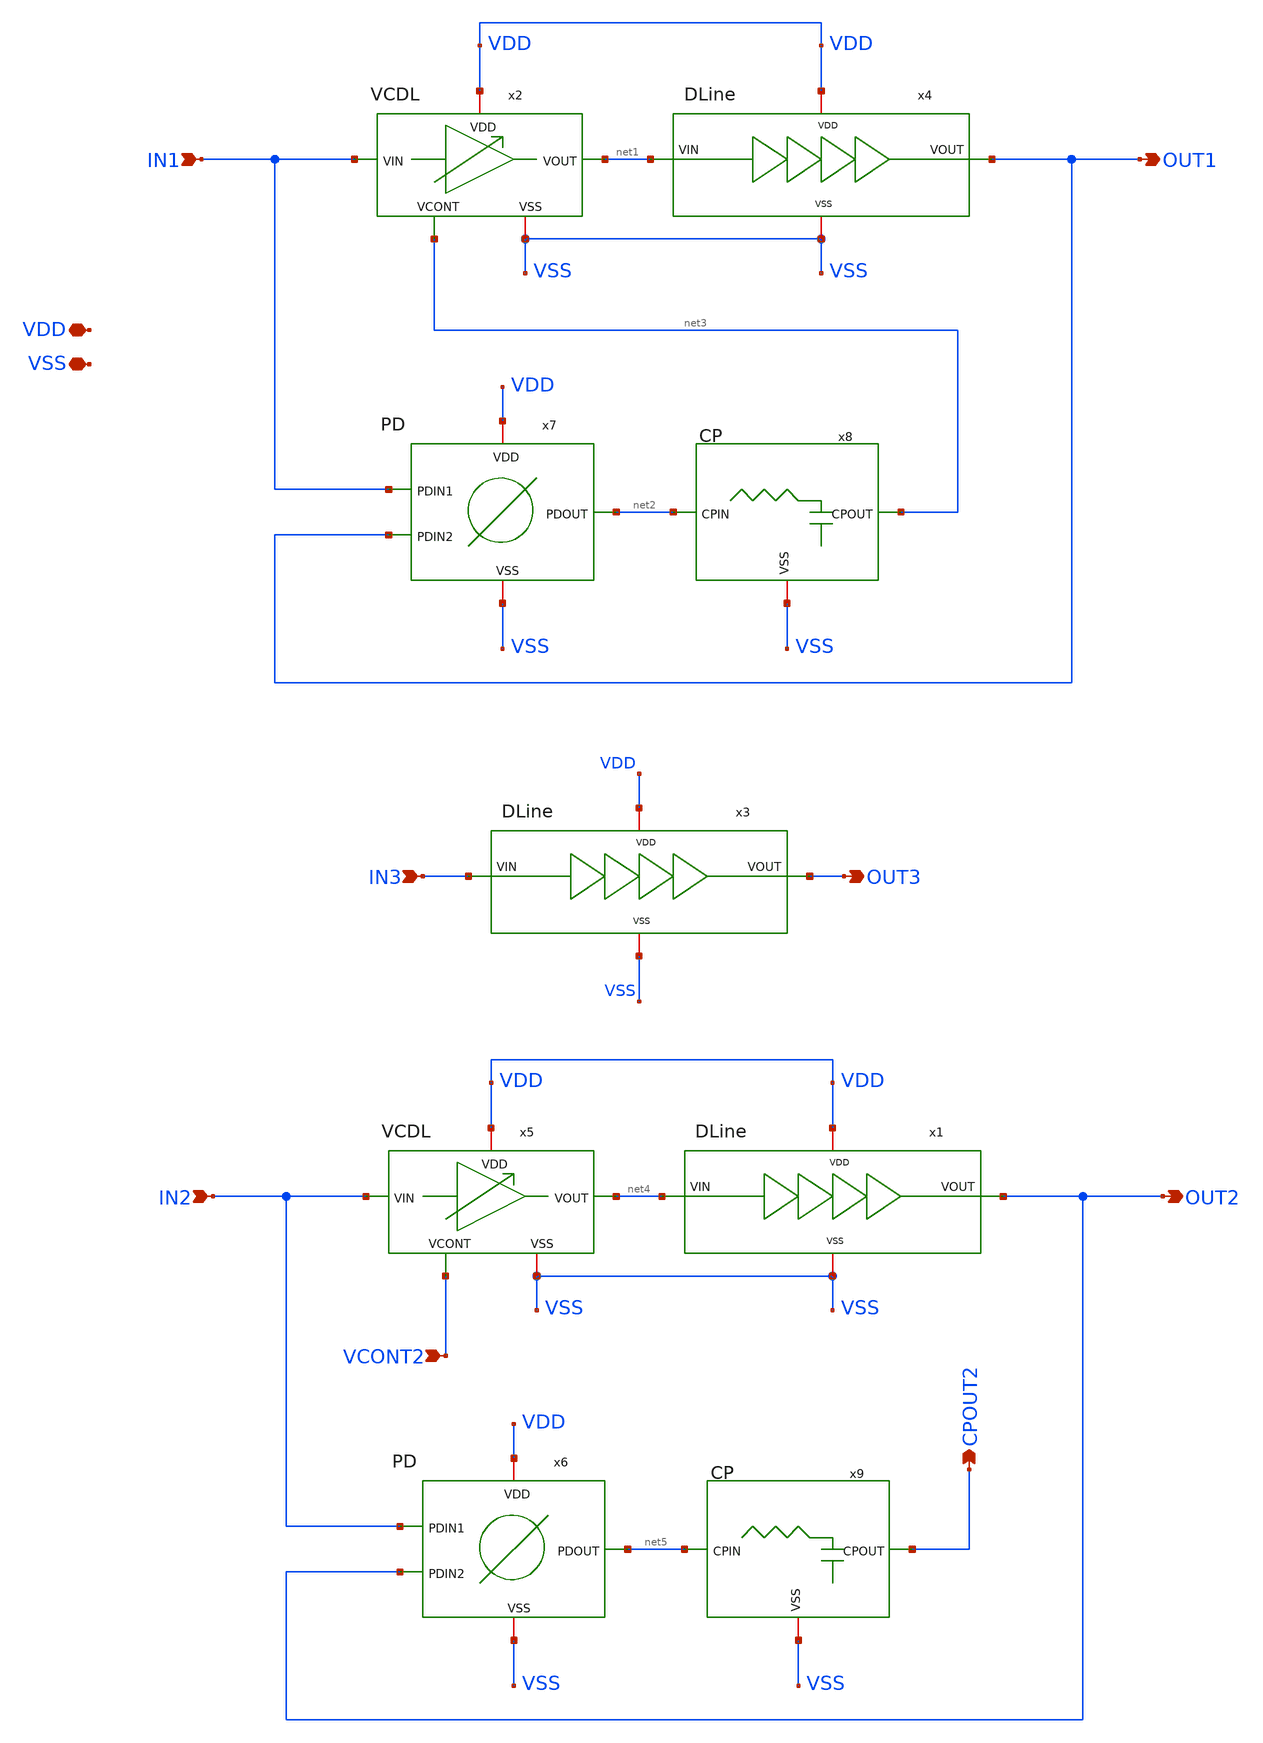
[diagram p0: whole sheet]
** sch_path: QDLL6501-main/schematic/xschem/QDLL_TOP.sch
* IHP-GmbH/IHP-Open-PDK/ihp-sg13g2/libs.tech/xschem/sg13g2_stdcells/sg13g2_dlygate4sd2_1.sch:
* Copyright 2023 IHP PDK Authors
* Licensed under the Apache License, Version 2.0 (the "License");
**.subckt QDLL_TOP VDD VSS IN1 IN2 OUT1 OUT2 CPOUT2 VCONT2 OUT3 IN3
*.iopin VDD
*.iopin VSS
*.ipin IN1
*.ipin IN2
*.opin OUT1
*.opin OUT2
*.opin CPOUT2
*.ipin VCONT2
*.opin OUT3
*.ipin IN3
x2 VDD IN1 net1 net3 VSS VCDL
x5 VDD IN2 net4 VCONT2 VSS VCDL
x1 VSS VDD net4 OUT2 DLine
x3 VSS VDD IN3 OUT3 DLine
x4 VSS VDD net1 OUT1 DLine
x6 VDD VSS IN2 net5 OUT2 PD
x7 VDD VSS IN1 net2 OUT1 PD
x8 net2 net3 VSS CP
x9 net5 CPOUT2 VSS CP
**.ends

* expanding   symbol:
*+  IHP__MPC0349/dependencies/IHP__QDLL6501/QDLL6501-main/schematic/xschem/VCDL.sym # of pins=5
** sym_path: QDLL6501-main/schematic/xschem/VCDL.sym
** sch_path: QDLL6501-main/schematic/xschem/VCDL.sch
.subckt VCDL VDD VIN VOUT VCONT VSS
*.iopin VDD
*.iopin VSS
*.ipin VIN
*.ipin VCONT
*.opin VOUT
XM1 VOUT VIN net3 VSS sg13_lv_nmos w=2u l=0.13u ng=1 m=1 mm_ok=1
XM2 net3 VCONT VSS VSS sg13_lv_nmos w=3.5u l=0.18u ng=1 m=1 mm_ok=1
XM3 net1 VCONT VSS VSS sg13_lv_nmos w=2u l=0.25u ng=1 m=1 mm_ok=1
XM4 VOUT VIN net2 VDD sg13_lv_pmos w=4.46u l=0.13u ng=1 m=1 mm_ok=1
XM5 net2 net1 VDD VDD sg13_lv_pmos w=2.24u l=0.13u ng=1 m=1 mm_ok=1
XM6 net1 net1 VDD VDD sg13_lv_pmos w=2.24u l=0.13u ng=1 m=1 mm_ok=1
.ends


* expanding   symbol:
*+  IHP__MPC0349/dependencies/IHP__QDLL6501/QDLL6501-main/schematic/xschem/DLine.sym # of pins=4
** sym_path: QDLL6501-main/schematic/xschem/DLine.sym
** sch_path: QDLL6501-main/schematic/xschem/DLine.sch
.subckt DLine VSS VDD VIN VOUT
*.opin VOUT
*.ipin VIN
*.iopin VDD
*.iopin VSS
x2 net1 net4 VDD VSS sg13g2_inv_4
x3 net2 net1 VDD VSS sg13g2_inv_8
x4 VOUT net2 VDD VSS sg13g2_inv_16
x5 net3 VIN VDD VSS sg13g2_dlygate4sd3_1
x6 net4 net3 VDD VSS sg13g2_dlygate4sd2_1
.ends


* expanding   symbol:  IHP__MPC0349/dependencies/IHP__QDLL6501/QDLL6501-main/schematic/xschem/PD.sym
*+ # of pins=5
** sym_path: QDLL6501-main/schematic/xschem/PD.sym
** sch_path: QDLL6501-main/schematic/xschem/PD.sch
.subckt PD VDD VSS PDIN1 PDOUT PDIN2
*.iopin VDD
*.iopin VSS
*.opin PDOUT
*.ipin PDIN1
*.ipin PDIN2
x1 PDOUT PDIN1 PDIN2 VDD VSS sg13g2_xor2_1
.ends


* expanding   symbol:  IHP__MPC0349/dependencies/IHP__QDLL6501/QDLL6501-main/schematic/xschem/CP.sym
*+ # of pins=3
** sym_path: QDLL6501-main/schematic/xschem/CP.sym
** sch_path: QDLL6501-main/schematic/xschem/CP.sch
.subckt CP CPIN CPOUT VSS
*.iopin VSS
*.ipin CPIN
*.opin CPOUT
XC1 CPOUT VSS cap_cmim w=60e-6 l=20e-6 m=1 mm_ok=1
x1 CPOUT CPIN RES
.ends


* expanding   symbol:  sg13g2_stdcells/sg13g2_inv_2.sym # of pins=2
** sym_path: sg13g2_stdcells/sg13g2_inv_2.sym
** sch_path: sg13g2_stdcells/sg13g2_inv_2.sch
.subckt sg13g2_inv_2 Y A VDD VSS
*.opin Y
*.ipin A
*.iopin VDD
*.iopin VSS
XM1 Y A VSS VSS sg13_lv_nmos w=1.48u l=130.00n ng=2 m=1 mm_ok=1
XM2 Y A VDD VDD sg13_lv_pmos w=2.24u l=130.00n ng=2 m=1 mm_ok=1
.ends


* expanding   symbol:  sg13g2_stdcells/sg13g2_inv_4.sym # of pins=2
** sym_path: sg13g2_stdcells/sg13g2_inv_4.sym
** sch_path: sg13g2_stdcells/sg13g2_inv_4.sch
.subckt sg13g2_inv_4 Y A VDD VSS
*.ipin A
*.opin Y
*.iopin VDD
*.iopin VSS
XM1 Y A VSS VSS sg13_lv_nmos w=2.96u l=130.00n ng=4 m=1 mm_ok=1
XM2 Y A VDD VDD sg13_lv_pmos w=4.48u l=130.00n ng=4 m=1 mm_ok=1
.ends


* expanding   symbol:  sg13g2_stdcells/sg13g2_inv_8.sym # of pins=2
** sym_path: sg13g2_stdcells/sg13g2_inv_8.sym
** sch_path: sg13g2_stdcells/sg13g2_inv_8.sch
.subckt sg13g2_inv_8 Y A VDD VSS
*.opin Y
*.ipin A
*.iopin VDD
*.iopin VSS
XM1 Y A VSS VSS sg13_lv_nmos w=5.92u l=130.00n ng=8 m=1 mm_ok=1
XM2 Y A VDD VDD sg13_lv_pmos w=8.96u l=130.00n ng=8 m=1 mm_ok=1
.ends


* expanding   symbol:  sg13g2_stdcells/sg13g2_inv_16.sym # of pins=2
** sym_path: sg13g2_stdcells/sg13g2_inv_16.sym
** sch_path: sg13g2_stdcells/sg13g2_inv_16.sch
.subckt sg13g2_inv_16 Y A VDD VSS
*.opin Y
*.iopin VSS
*.ipin A
*.iopin VDD
XM1 Y A VSS VSS sg13_lv_nmos w=11.84u l=130.00n ng=16 m=1 mm_ok=1
XM2 Y A VDD VDD sg13_lv_pmos w=17.92u l=130.00n ng=16 m=1 mm_ok=1
.ends


* expanding   symbol:  sg13g2_stdcells/sg13g2_dlygate4sd3_1.sym # of pins=2
** sym_path: sg13g2_stdcells/sg13g2_dlygate4sd3_1.sym
** sch_path: sg13g2_stdcells/sg13g2_dlygate4sd3_1.sch
.subckt sg13g2_dlygate4sd3_1 X A VDD VSS
*.ipin A
*.opin X
*.iopin VDD
*.iopin VSS
XM1 net3 A VSS VSS sg13_lv_nmos w=420.00n l=130.00n ng=1 m=1 mm_ok=1
XM2 net1 net3 VSS VSS sg13_lv_nmos w=420.00n l=500.0n ng=1 m=1 mm_ok=1
XM3 net2 net1 VSS VSS sg13_lv_nmos w=420.00n l=500.0n ng=1 m=1 mm_ok=1
XM4 X net2 VSS VSS sg13_lv_nmos w=740.00n l=130.00n ng=1 m=1 mm_ok=1
XM5 net3 A VDD VDD sg13_lv_pmos w=420.00n l=130.00n ng=1 m=1 mm_ok=1
XM6 net1 net3 VDD VDD sg13_lv_pmos w=1.000u l=500.0n ng=1 m=1 mm_ok=1
XM7 net2 net1 VDD VDD sg13_lv_pmos w=1.000u l=500.0n ng=1 m=1 mm_ok=1
XM8 X net2 VDD VDD sg13_lv_pmos w=1.12u l=130.00n ng=1 m=1 mm_ok=1
.ends


* expanding   symbol:  sg13g2_stdcells/sg13g2_dlygate4sd2_1.sym # of pins=2
** sym_path: sg13g2_stdcells/sg13g2_dlygate4sd2_1.sym
** sch_path: sg13g2_stdcells/sg13g2_dlygate4sd2_1.sch
.subckt sg13g2_dlygate4sd2_1 X A VDD VSS
*.ipin A
*.opin X
*.iopin VDD
*.iopin VSS
XM1 net2 A VSS VSS sg13_lv_nmos w=420.00n l=130.00n ng=1 m=1 mm_ok=1
XM2 net1 net2 VSS VSS sg13_lv_nmos w=420.00n l=180.00n ng=1 m=1 mm_ok=1
XM3 net3 net1 VSS VSS sg13_lv_nmos w=420.00n l=180.00n ng=1 m=1 mm_ok=1
XM4 X net3 VSS VSS sg13_lv_nmos w=740.00n l=130.00n ng=1 m=1 mm_ok=1
XM5 net2 A VDD VDD sg13_lv_pmos w=420.00n l=130.00n ng=1 m=1 mm_ok=1
XM6 net1 net2 VDD VDD sg13_lv_pmos w=1.000u l=250.00n ng=1 m=1 mm_ok=1
XM7 net3 net1 VDD VDD sg13_lv_pmos w=1.000u l=250.00n ng=1 m=1 mm_ok=1
XM8 X net3 VDD VDD sg13_lv_pmos w=1.12u l=130.00n ng=1 m=1 mm_ok=1
.ends


* expanding   symbol:  sg13g2_stdcells/sg13g2_xor2_1.sym # of pins=3
** sym_path: sg13g2_stdcells/sg13g2_xor2_1.sym
** sch_path: sg13g2_stdcells/sg13g2_xor2_1.sch
.subckt sg13g2_xor2_1 X A B VDD VSS
*.opin X
*.ipin B
*.ipin A
*.iopin VDD
*.iopin VSS
XM1 net1 A VSS VSS sg13_lv_nmos w=550.00n l=130.00n ng=1 m=1 mm_ok=1
XM2 net1 B VSS VSS sg13_lv_nmos w=550.00n l=130.00n ng=1 m=1 mm_ok=1
XM3 X net1 VSS VSS sg13_lv_nmos w=740.00n l=130.00n ng=1 m=1 mm_ok=1
XM4 X B net3 VSS sg13_lv_nmos w=740.00n l=130.00n ng=1 m=1 mm_ok=1
XM5 net3 A VSS VSS sg13_lv_nmos w=740.00n l=130.00n ng=1 m=1 mm_ok=1
XM6 net4 A VDD VDD sg13_lv_pmos w=1.000u l=130.00n ng=1 m=1 mm_ok=1
XM7 net1 B net4 VDD sg13_lv_pmos w=1.000u l=130.00n ng=1 m=1 mm_ok=1
XM8 net2 A VDD VDD sg13_lv_pmos w=1.12u l=130.00n ng=1 m=1 mm_ok=1
XM9 X net1 net2 VDD sg13_lv_pmos w=1.12u l=130.00n ng=1 m=1 mm_ok=1
XM10 net2 B VDD VDD sg13_lv_pmos w=1.12u l=130.00n ng=1 m=1 mm_ok=1
.ends


* expanding   symbol:
*+  IHP__MPC0349/dependencies/IHP__QDLL6501/QDLL6501-main/schematic/xschem/RES.sym # of pins=2
** sym_path: QDLL6501-main/schematic/xschem/RES.sym
** sch_path: QDLL6501-main/schematic/xschem/RES.sch
.subckt RES ROUT RIN
*.ipin RIN
*.opin ROUT
XR13 net1 RIN VSS rppd w=1e-6 l=10e-6 m=1 b=0 mm_ok=1
XR1 net2 net1 VSS rppd w=1e-6 l=10e-6 m=1 b=0 mm_ok=1
XR2 net3 net2 VSS rppd w=1e-6 l=10e-6 m=1 b=0 mm_ok=1
XR3 net4 net3 VSS rppd w=1e-6 l=10e-6 m=1 b=0 mm_ok=1
XR4 net5 net4 VSS rppd w=1e-6 l=10e-6 m=1 b=0 mm_ok=1
XR5 net6 net5 VSS rppd w=1e-6 l=10e-6 m=1 b=0 mm_ok=1
XR6 net7 net6 VSS rppd w=1e-6 l=10e-6 m=1 b=0 mm_ok=1
XR7 net8 net7 VSS rppd w=1e-6 l=10e-6 m=1 b=0 mm_ok=1
XR8 net9 net8 VSS rppd w=1e-6 l=10e-6 m=1 b=0 mm_ok=1
XR9 net10 net9 VSS rppd w=1e-6 l=10e-6 m=1 b=0 mm_ok=1
XR10 net11 net10 VSS rppd w=1e-6 l=10e-6 m=1 b=0 mm_ok=1
XR11 ROUT net11 VSS rppd w=1e-6 l=10e-6 m=1 b=0 mm_ok=1
.ends

.end
